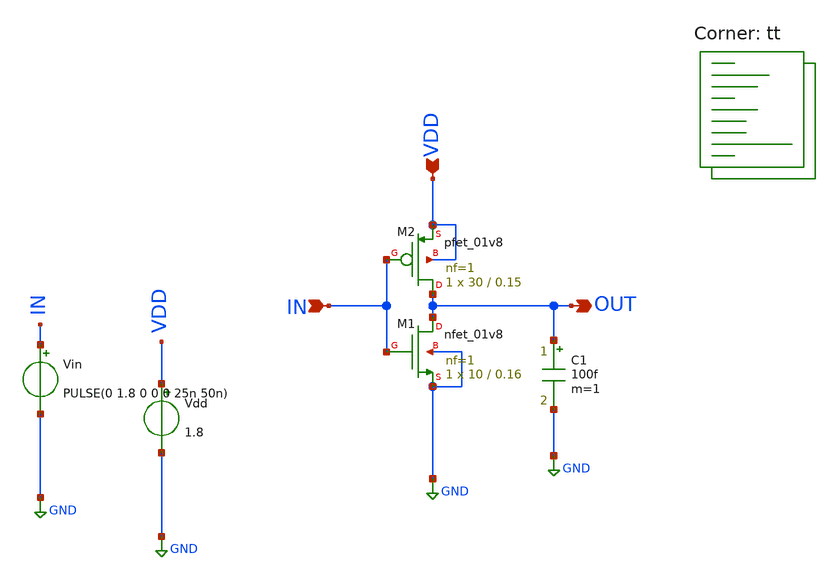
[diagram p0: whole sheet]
** sch_path: sizing-inverter.sch
**.subckt sizing-inverter IN VDD OUT
*.ipin IN
*.ipin VDD
*.opin OUT
Vin IN GND PULSE(0 1.8 0 0 0 25n 50n)
Vdd VDD GND 1.8
XM1 OUT IN GND GND sky130_fd_pr__nfet_01v8 L=0.16 W=10 nf=1 ad='int((nf+1)/2) * W/nf * 0.29' as='int((nf+2)/2) * W/nf * 0.29'
+ pd='2*int((nf+1)/2) * (W/nf + 0.29)' ps='2*int((nf+2)/2) * (W/nf + 0.29)' nrd='0.29 / W' nrs='0.29 / W'
+ sa=0 sb=0 sd=0 mult=1 m=1
XM2 OUT IN VDD VDD sky130_fd_pr__pfet_01v8 L=0.15 W=30 nf=1 ad='int((nf+1)/2) * W/nf * 0.29' as='int((nf+2)/2) * W/nf * 0.29'
+ pd='2*int((nf+1)/2) * (W/nf + 0.29)' ps='2*int((nf+2)/2) * (W/nf + 0.29)' nrd='0.29 / W' nrs='0.29 / W'
+ sa=0 sb=0 sd=0 mult=1 m=1
C1 OUT GND 100f m=1
**** begin user architecture code
.lib $::SKYWATER_MODELS/sky130.lib.spice tt


.options savecurrents

.control
save all

foreach nmos_w 10 20
  alter @m.xm1.msky130_fd_pr__nfet_01v8[w]=$nmos_w

  let step=1
  let final_w_pmos=50
  let current_w_pmos=10

  let total_iterations = ceil((final_w_pmos - current_w_pmos)/step)
  let index= 0

  let switching_points = vector(total_iterations)
  let asymmetricity = vector(total_iterations)
  let width = vector(total_iterations)


  while current_w_pmos < final_w_pmos

    alter m.xm2.msky130_fd_pr__pfet_01v8 W=current_w_pmos

  ******* Asymmetricity analysis ********
    tran 10p 50n ; Run transient analysis using a symmetric pulse of period 25n

    meas tran rise_time TRIG v(out) VAL=0.1 RISE=1 TARG v(out) VAL=1.62 RISE=1
    meas tran fall_time TRIG v(out) VAL=1.62 FALL=1 TARG v(out) VAL=0.1 FALL=1

    let asymmetricity[index] = abs( $&rise_time - $&fall_time ) ; Create array of diffs



  ******* Switching point analysis ********
    dc vin 0 1.8 1m ; Run dc analysis, check for operating point

    meas dc switching_point WHEN v(out)=v(in) CROSS=LAST
    set plotstr = ( $plotstr {$curplot}.v(out) )
    set global_switching_point = $&switching_point

    let switching_points[index] = $&switching_point
    let width[index] = current_w_pmos


    let current_w_pmos=current_w_pmos + step
    let index=index + 1

  end

  set plotstr = ( $plotstr {$curplot}.v(in) )

  set nolegend

  ******* Plot results ********
  plot switching_points vs width title 'switching points vs time' xlabel 'width' ylabel 'Switching point (V)'
  plot asymmetricity vs width title 'asymmetricity vs time' xlabel 'width' ylabel 'Difference in rise/fall'

  plot $plotstr

  ******* Find switching point at most symmetric w ********
  let lowest_asym = 100
  let best_w_index = 0 ; Find most symmetric w
  let index = 0
  let tolerance = 1p ; We let the asymmetricity be plus/minus 1p of 0

  repeat $&total_iterations

    let asym = abs(asymmetricity[index] - 1p)
    let current_w_pmos = width[index]

    if asym < lowest_asym ; If we have something smaller, set it as the best goal and repeat
      let best_w_index = index
      let lowest_asym = asym

    end

    let index = index + 1
  end

  * Now that we have the best width, we now need to move towards getting the switching point

  let chosen_switching_point = switching_points[best_w_index]

end

.endc


**** end user architecture code
**.ends
.GLOBAL GND
.end
